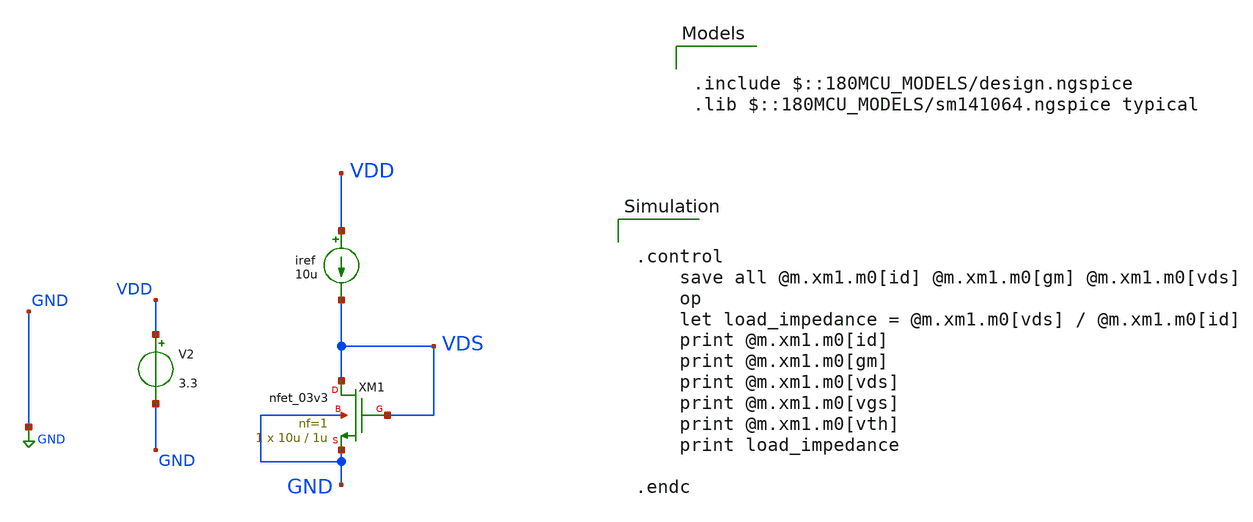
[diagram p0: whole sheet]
** sch_path: designs/libs/session_2/diode_connected_nmos.sch
**.subckt diode_connected_nmos
XM1 VDS VDS GND GND nfet_03v3 L=1u W=10u nf=1 ad='int((nf+1)/2) * W/nf * 0.18u' as='int((nf+2)/2) * W/nf * 0.18u'
+ pd='2*int((nf+1)/2) * (W/nf + 0.18u)' ps='2*int((nf+2)/2) * (W/nf + 0.18u)' nrd='0.18u / W' nrs='0.18u / W'
+ sa=0 sb=0 sd=0 m=1
iref VDD VDS 10u
V2 VDD GND 3.3
**** begin user architecture code

.include $::180MCU_MODELS/design.ngspice
.lib $::180MCU_MODELS/sm141064.ngspice typical



.control
    save all @m.xm1.m0[id] @m.xm1.m0[gm] @m.xm1.m0[vds]
    op
    let load_impedance = @m.xm1.m0[vds] / @m.xm1.m0[id]
    print @m.xm1.m0[id]
    print @m.xm1.m0[gm]
    print @m.xm1.m0[vds]
    print @m.xm1.m0[vgs]
    print @m.xm1.m0[vth]
    print load_impedance

.endc


**** end user architecture code
**.ends
.GLOBAL GND
.end
